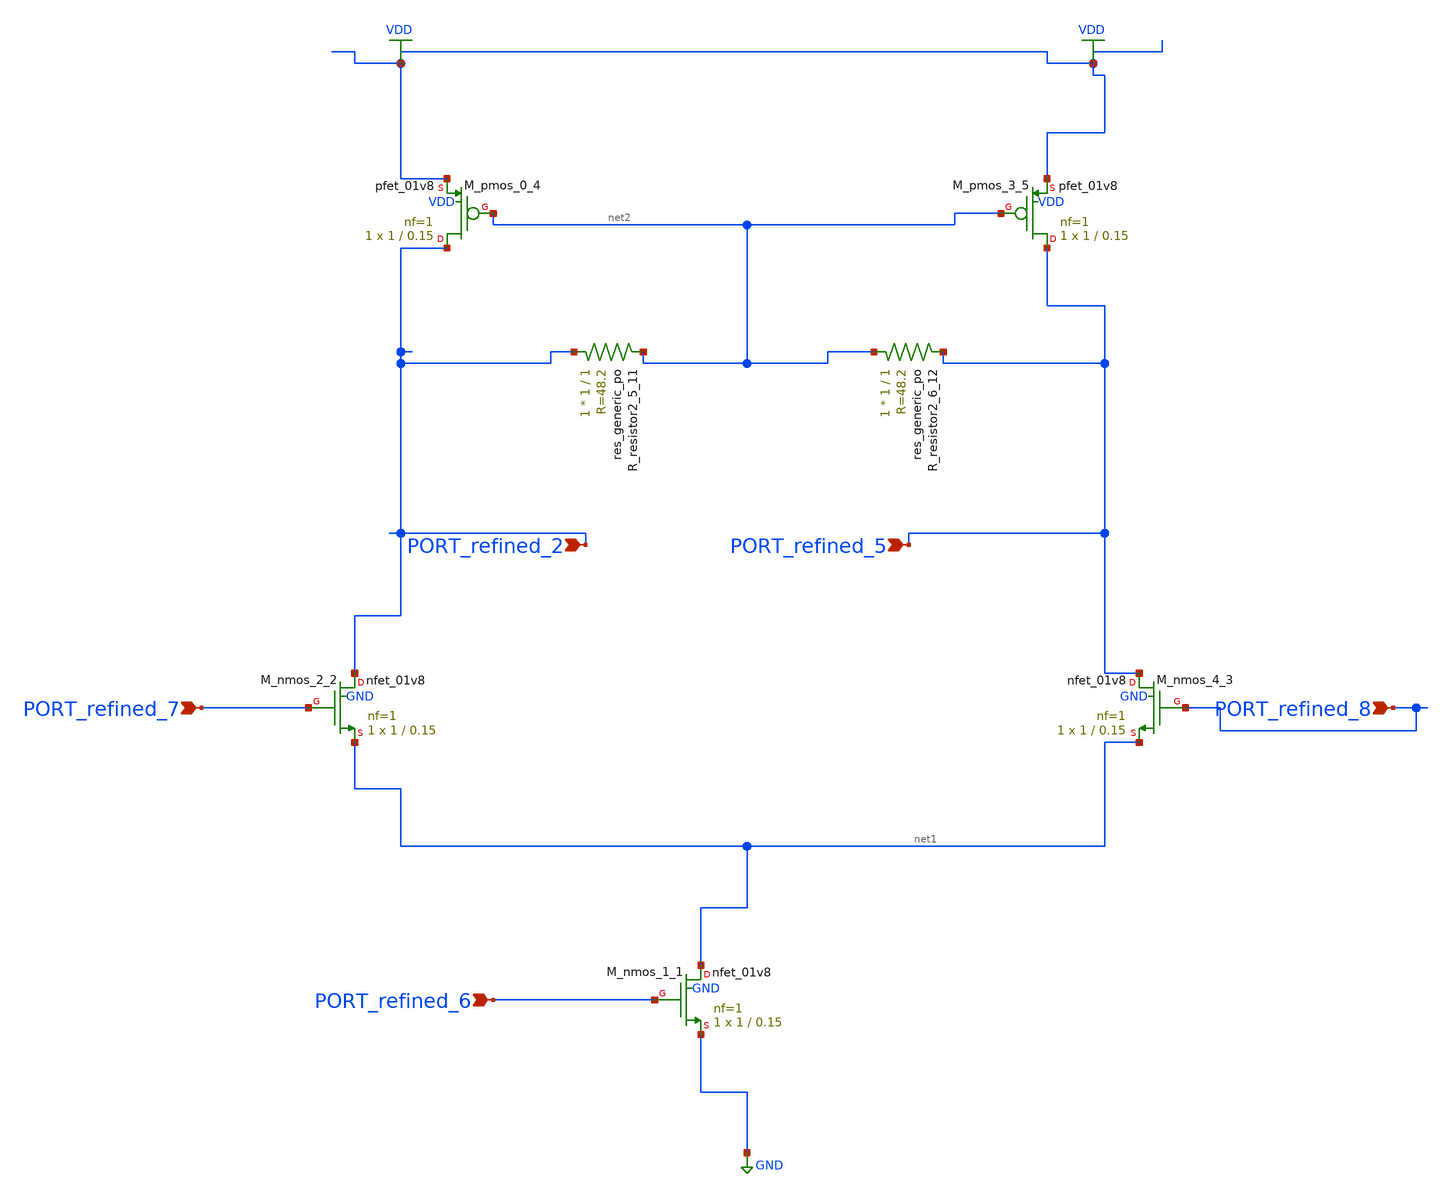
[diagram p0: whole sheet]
** sch_path: schematics/AMSNet/240.sch
**.subckt 240 PORT_refined_2 PORT_refined_5 PORT_refined_8 PORT_refined_6 PORT_refined_7
*.ipin PORT_refined_2
*.ipin PORT_refined_5
*.ipin PORT_refined_8
*.ipin PORT_refined_6
*.ipin PORT_refined_7
XM_nmos_1_1 net1 PORT_refined_6 GND GND sky130_fd_pr__nfet_01v8 L=0.15 W=1 nf=1 ad='int((1 + 1)/2) * 1 / 1 * 0.29'
+ as='int((1 + 2)/2) * 1 / 1 * 0.29' pd='2*int((1 + 1)/2) * (1 / 1 + 0.29)' ps='2*int((1 + 2)/2) * (1 / 1 + 0.29)'
+ nrd='0.29 / 1 ' nrs='0.29 / 1 ' sa=0 sb=0 sd=0 mult=1 m=1
XM_nmos_2_2 PORT_refined_2 PORT_refined_7 net1 GND sky130_fd_pr__nfet_01v8 L=0.15 W=1 nf=1 ad='int((1 + 1)/2) * 1 / 1 * 0.29'
+ as='int((1 + 2)/2) * 1 / 1 * 0.29' pd='2*int((1 + 1)/2) * (1 / 1 + 0.29)' ps='2*int((1 + 2)/2) * (1 / 1 + 0.29)'
+ nrd='0.29 / 1 ' nrs='0.29 / 1 ' sa=0 sb=0 sd=0 mult=1 m=1
XM_nmos_4_3 PORT_refined_5 PORT_refined_8 net1 GND sky130_fd_pr__nfet_01v8 L=0.15 W=1 nf=1 ad='int((1 + 1)/2) * 1 / 1 * 0.29'
+ as='int((1 + 2)/2) * 1 / 1 * 0.29' pd='2*int((1 + 1)/2) * (1 / 1 + 0.29)' ps='2*int((1 + 2)/2) * (1 / 1 + 0.29)'
+ nrd='0.29 / 1 ' nrs='0.29 / 1 ' sa=0 sb=0 sd=0 mult=1 m=1
XM_pmos_0_4 PORT_refined_2 net2 VDD VDD sky130_fd_pr__pfet_01v8 L=0.15 W=1 nf=1 ad='int((1 + 1)/2) * 1 / 1 * 0.29'
+ as='int((1 + 2)/2) * 1 / 1 * 0.29' pd='2*int((1 + 1)/2) * (1 / 1 + 0.29)' ps='2*int((1 + 2)/2) * (1 / 1 + 0.29)'
+ nrd='0.29 / 1 ' nrs='0.29 / 1 ' sa=0 sb=0 sd=0 mult=1 m=1
XM_pmos_3_5 PORT_refined_5 net2 VDD VDD sky130_fd_pr__pfet_01v8 L=0.15 W=1 nf=1 ad='int((1 + 1)/2) * 1 / 1 * 0.29'
+ as='int((1 + 2)/2) * 1 / 1 * 0.29' pd='2*int((1 + 1)/2) * (1 / 1 + 0.29)' ps='2*int((1 + 2)/2) * (1 / 1 + 0.29)'
+ nrd='0.29 / 1 ' nrs='0.29 / 1 ' sa=0 sb=0 sd=0 mult=1 m=1
XR_resistor2_5_11 PORT_refined_2 net2 sky130_fd_pr__res_generic_po W=1 L=1 m=1
XR_resistor2_6_12 net2 PORT_refined_5 sky130_fd_pr__res_generic_po W=1 L=1 m=1
**.ends
.GLOBAL GND
.GLOBAL VDD
.end
